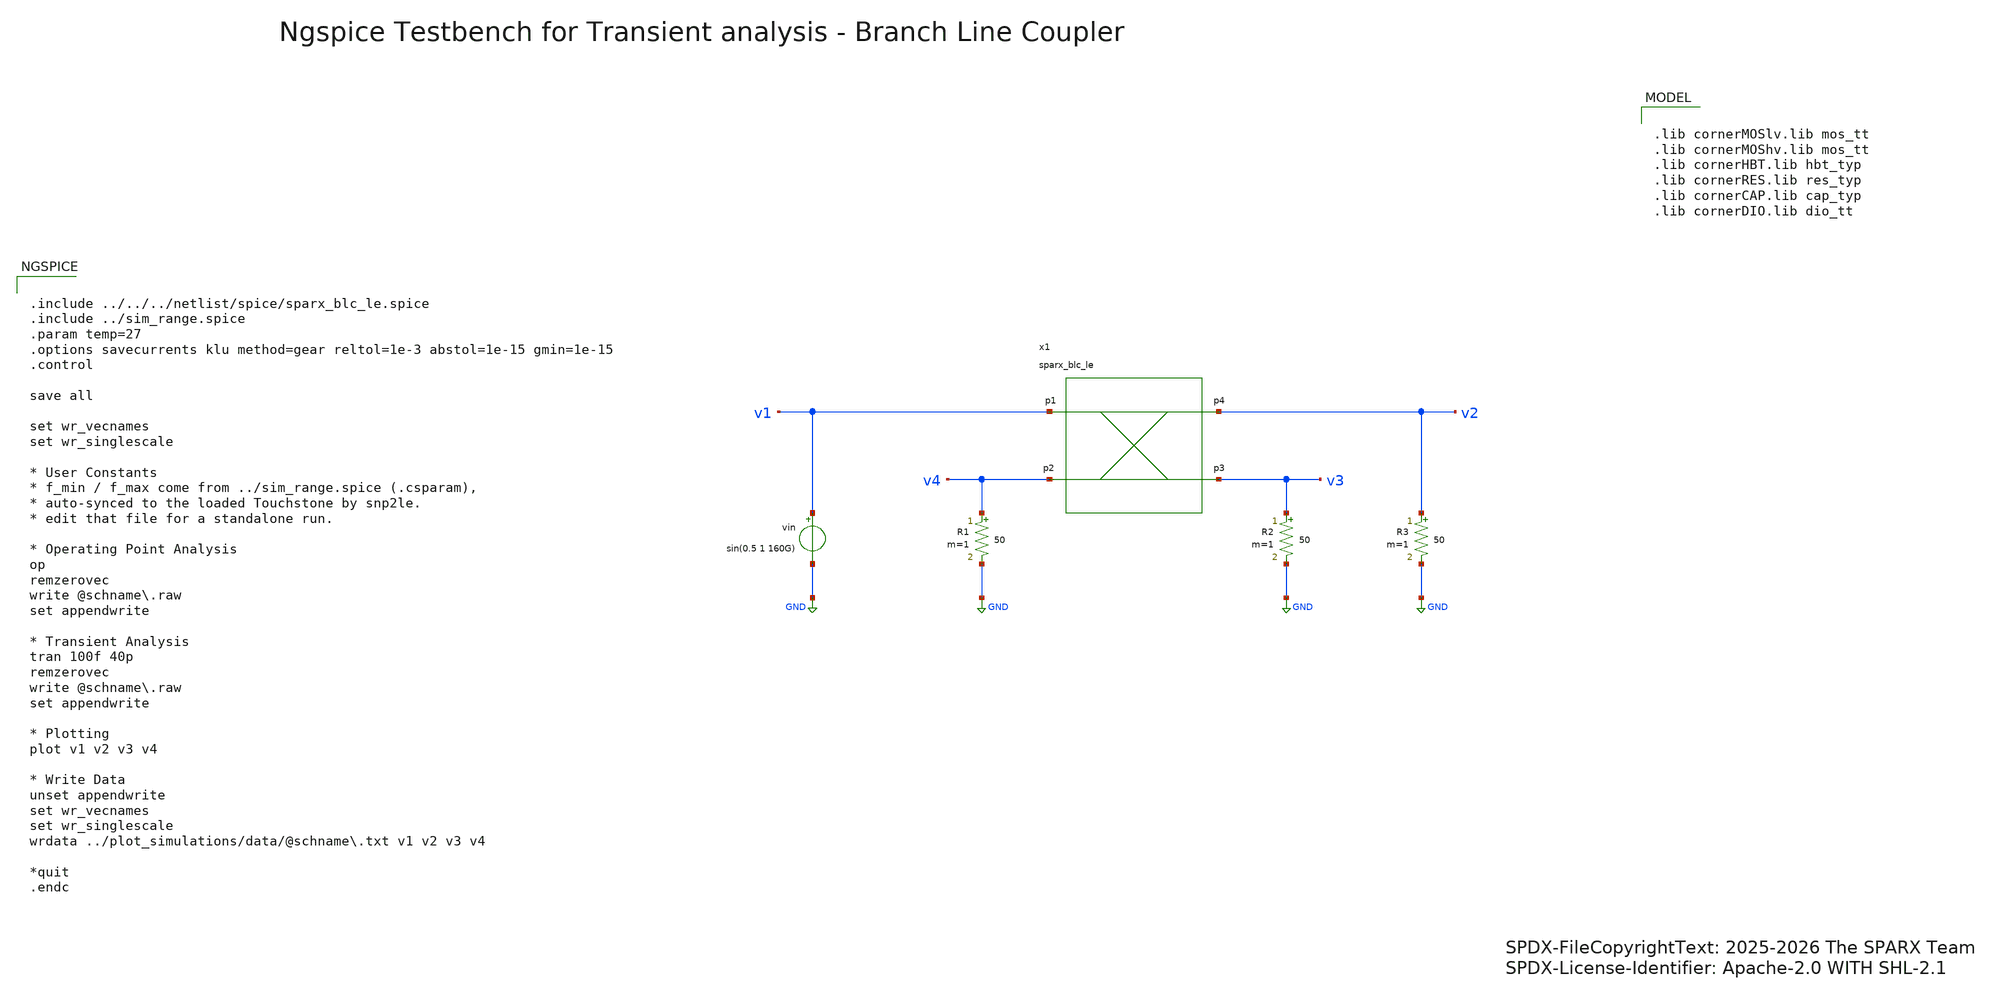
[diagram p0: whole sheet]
** sch_path: testbenches/xschem/sparx_blc_le_tb_tran_ngspice.sch
* SPDX-FileCopyrightText: 2025-2026 The SPARX Team
* SPDX-License-Identifier: Apache-2.0 WITH SHL-2.1
**.subckt sparx_blc_le_tb_tran_ngspice
vin v1 GND sin(0.5 1 160G)
x1 v1 v4 v3 v2 sparx_blc_le
R1 v4 GND 50 m=1
R2 v3 GND 50 m=1
R3 v2 GND 50 m=1
**** begin user architecture code


.include ../../../netlist/spice/sparx_blc_le.spice
.include ../sim_range.spice
.param temp=27
.options savecurrents klu method=gear reltol=1e-3 abstol=1e-15 gmin=1e-15
.control

save all

set wr_vecnames
set wr_singlescale

* User Constants
* f_min / f_max come from ../sim_range.spice (.csparam),
* auto-synced to the loaded Touchstone by snp2le.
* edit that file for a standalone run.

* Operating Point Analysis
op
remzerovec
write @schname\.raw
set appendwrite

* Transient Analysis
tran 100f 40p
remzerovec
write @schname\.raw
set appendwrite

* Plotting
plot v1 v2 v3 v4

* Write Data
unset appendwrite
set wr_vecnames
set wr_singlescale
wrdata ../plot_simulations/data/@schname\.txt v1 v2 v3 v4

*quit
.endc



.lib cornerMOSlv.lib mos_tt
.lib cornerMOShv.lib mos_tt
.lib cornerHBT.lib hbt_typ
.lib cornerRES.lib res_typ
.lib cornerCAP.lib cap_typ
.lib cornerDIO.lib dio_tt

**** end user architecture code
**.ends
.GLOBAL GND
.end
